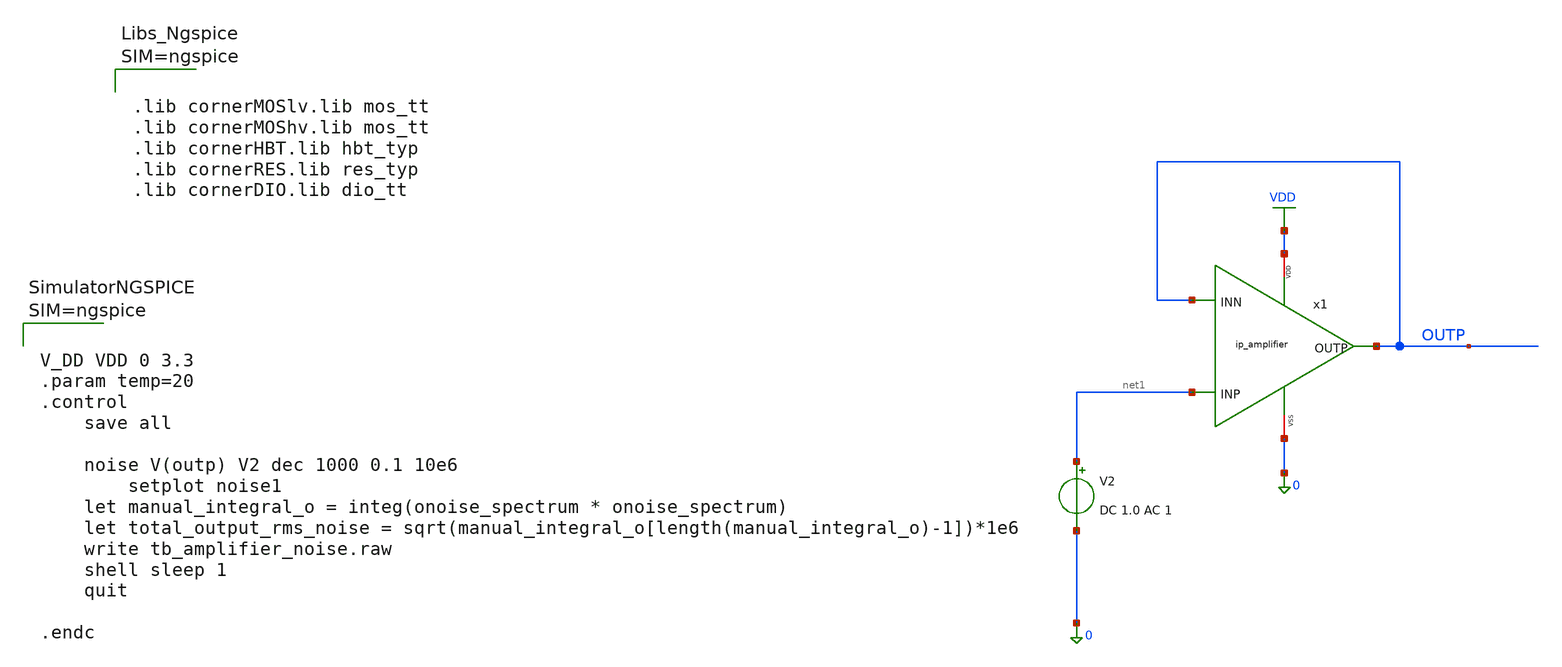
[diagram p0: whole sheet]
** sch_path: xschem/tb_amplifier_noise.sch
**.subckt tb_amplifier_noise
x1 VDD OUTP OUTP net1 0 ip_amplifier
V2 net1 0 DC 1.0 AC 1
**** begin user architecture code



.lib cornerMOSlv.lib mos_tt
.lib cornerMOShv.lib mos_tt
.lib cornerHBT.lib hbt_typ
.lib cornerRES.lib res_typ
.lib cornerDIO.lib dio_tt






V_DD VDD 0 3.3
.param temp=20
.control
	save all

	noise V(outp) V2 dec 1000 0.1 10e6
        setplot noise1
	let manual_integral_o = integ(onoise_spectrum * onoise_spectrum)
	let total_output_rms_noise = sqrt(manual_integral_o[length(manual_integral_o)-1])*1e6
	write tb_amplifier_noise.raw
	shell sleep 1
	quit

.endc



**** end user architecture code
**.ends

* expanding   symbol:  ip_amplifier.sym # of pins=5
** sym_path: xschem/ip_amplifier.sym
** sch_path: xschem/ip_amplifier.sch
.subckt ip_amplifier VDD OUTP INN INP VSS
*.iopin VSS
*.iopin VDD
*.opin OUTP
*.ipin INN
*.ipin INP
XM1 net2 BIAS_N VSS VSS sg13_hv_nmos w=10u l=5u ng=1 m=1 mm_ok=1
R1 VDD net8 30k m=2
XM2 net1 BIAS_N VSS VSS sg13_hv_nmos w=10u l=5u ng=1 m=1 mm_ok=1
XM3 net5 BIAS_N net1 VSS sg13_hv_nmos w=10u l=0.5u ng=1 m=20 mm_ok=1
XM4 BIAS_N BIAS_N net2 VSS sg13_hv_nmos w=10u l=0.5u ng=1 m=20 mm_ok=1
Vmeas BIAS_P net5 0
Vmeas1 net6 net7 0
XM5 net6 BIAS_P net4 VDD sg13_hv_pmos w=10u l=0.5u ng=1 m=30 mm_ok=1
XM6 net4 BIAS_P VDD VDD sg13_hv_pmos w=10u l=5u ng=1 m=2 mm_ok=1
XM7 net3 BIAS_P VDD VDD sg13_hv_pmos w=10u l=5u ng=1 m=2 mm_ok=1
XM8 BIAS_P BIAS_P net3 VDD sg13_hv_pmos w=10u l=0.5u ng=1 m=30 mm_ok=1
Vmeas2 net8 BIAS_N 0
XM9 COMP INP net7 VDD sg13_hv_pmos w=10u l=5u ng=1 m=20 mm_ok=1
XM10 net9 INN net7 VDD sg13_hv_pmos w=10u l=5u ng=1 m=20 mm_ok=1
XM11 net9 net9 VSS VSS sg13_hv_nmos w=10u l=5u ng=1 m=10 mm_ok=1
XM12 COMP net9 VSS VSS sg13_hv_nmos w=10u l=5u ng=1 m=10 mm_ok=1
XM13 net10 BIAS_P VDD VDD sg13_hv_pmos w=10u l=0.5u ng=1 m=5 mm_ok=1
XM14 OUTP COMP VSS VSS sg13_hv_nmos w=10u l=0.5u ng=1 m=10 mm_ok=1
Vmeas3 net10 OUTP 0
.ends

.GLOBAL VDD
.end
